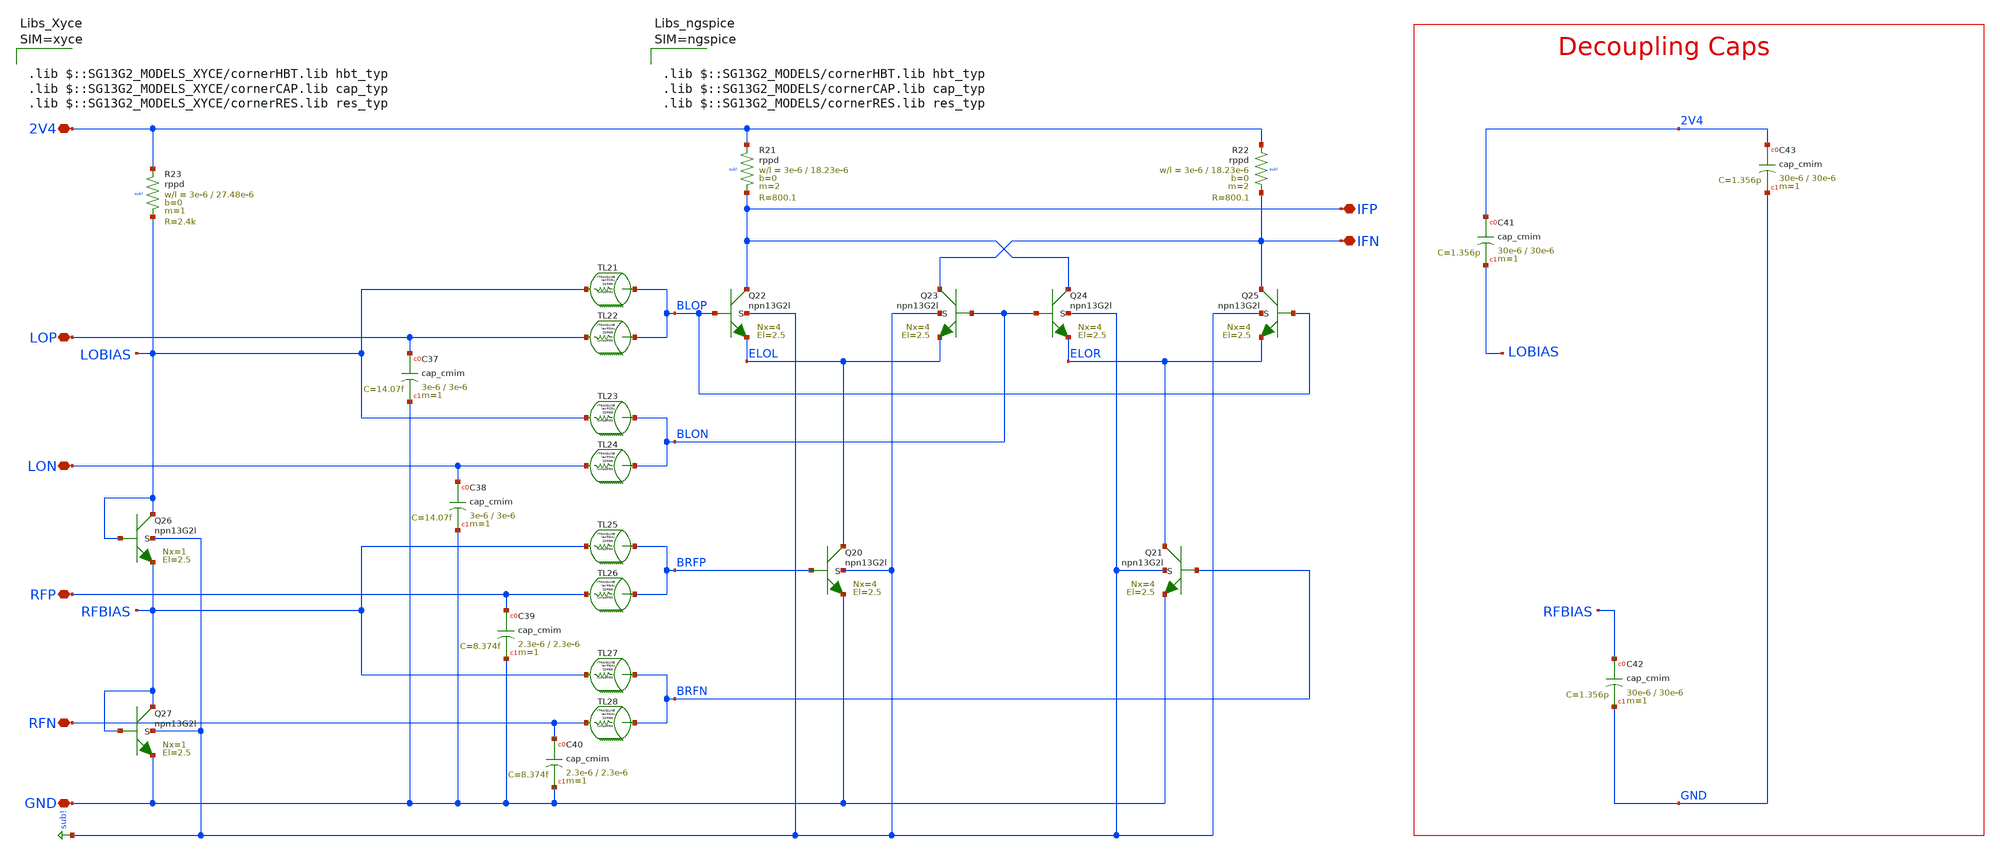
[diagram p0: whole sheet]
** sch_path: mWATTBAT/design_data/xschem/MIXER.sch
**.subckt MIXER 2V4 LOP LON RFP RFN GND IFP IFN
*.iopin 2V4
*.iopin LOP
*.iopin LON
*.iopin RFP
*.iopin RFN
*.iopin GND
*.iopin IFP
*.iopin IFN
XQ22 IFP BLOP ELOL sub! npn13G2l Nx=4 El=2.5 mm_ok=1
XQ23 IFN BLON ELOL sub! npn13G2l Nx=4 El=2.5 mm_ok=1
XQ24 IFP BLON ELOR sub! npn13G2l Nx=4 El=2.5 mm_ok=1
XQ25 IFN BLOP ELOR sub! npn13G2l Nx=4 El=2.5 mm_ok=1
XQ20 ELOL BRFP GND sub! npn13G2l Nx=4 El=2.5 mm_ok=1
XQ21 ELOR BRFN GND sub! npn13G2l Nx=4 El=2.5 mm_ok=1
XQ27 RFBIAS RFBIAS GND sub! npn13G2l Nx=1 El=2.5 mm_ok=1
XQ26 LOBIAS LOBIAS RFBIAS sub! npn13G2l Nx=1 El=2.5 mm_ok=1
ytransline TL23 BLON LOBIAS ytransline_TL23 len=25u lumps=50
.model ytransline_TL23 transline r=22.16k l=445.9n C=61.5p
ytransline TL21 BLOP LOBIAS ytransline_TL21 len=25u lumps=50
.model ytransline_TL21 transline r=22.16k l=445.9n C=61.5p
ytransline TL22 BLOP LOP ytransline_TL22 len=34u lumps=50
.model ytransline_TL22 transline r=22.16k l=445.9n C=61.5p
ytransline TL24 BLON LON ytransline_TL24 len=34u lumps=50
.model ytransline_TL24 transline r=22.16k l=445.9n C=61.5p
ytransline TL25 BRFP RFBIAS ytransline_TL25 len=64u lumps=50
.model ytransline_TL25 transline r=22.16k l=445.9n C=61.5p
ytransline TL27 BRFN RFBIAS ytransline_TL27 len=64u lumps=50
.model ytransline_TL27 transline r=22.16k l=445.9n C=61.5p
ytransline TL26 BRFP RFP ytransline_TL26 len=64u lumps=50
.model ytransline_TL26 transline r=22.16k l=445.9n C=61.5p
ytransline TL28 BRFN RFN ytransline_TL28 len=64u lumps=50
.model ytransline_TL28 transline r=22.16k l=445.9n C=61.5p
XR21 2V4 IFP sub! rppd w=3e-6 l=18.23e-6 m=2 b=0 mm_ok=1
XR22 2V4 IFN sub! rppd w=3e-6 l=18.23e-6 m=2 b=0 mm_ok=1
XC42 RFBIAS GND cap_cmim w=30e-6 l=30e-6 m=1 mm_ok=1
XC37 LOP GND cap_cmim w=3e-6 l=3e-6 m=1 mm_ok=1
XC38 LON GND cap_cmim w=3e-6 l=3e-6 m=1 mm_ok=1
XC39 RFP GND cap_cmim w=2.3e-6 l=2.3e-6 m=1 mm_ok=1
XC40 RFN GND cap_cmim w=2.3e-6 l=2.3e-6 m=1 mm_ok=1
XR23 2V4 LOBIAS sub! rppd w=3e-6 l=27.48e-6 m=1 b=0 mm_ok=1
XC41 2V4 LOBIAS cap_cmim w=30e-6 l=30e-6 m=1 mm_ok=1
XC43 2V4 GND cap_cmim w=30e-6 l=30e-6 m=1 mm_ok=1
**** begin user architecture code






.lib $::SG13G2_MODELS/cornerHBT.lib hbt_typ
.lib $::SG13G2_MODELS/cornerCAP.lib cap_typ
.lib $::SG13G2_MODELS/cornerRES.lib res_typ



**** end user architecture code
**.ends
.GLOBAL sub!
.end
